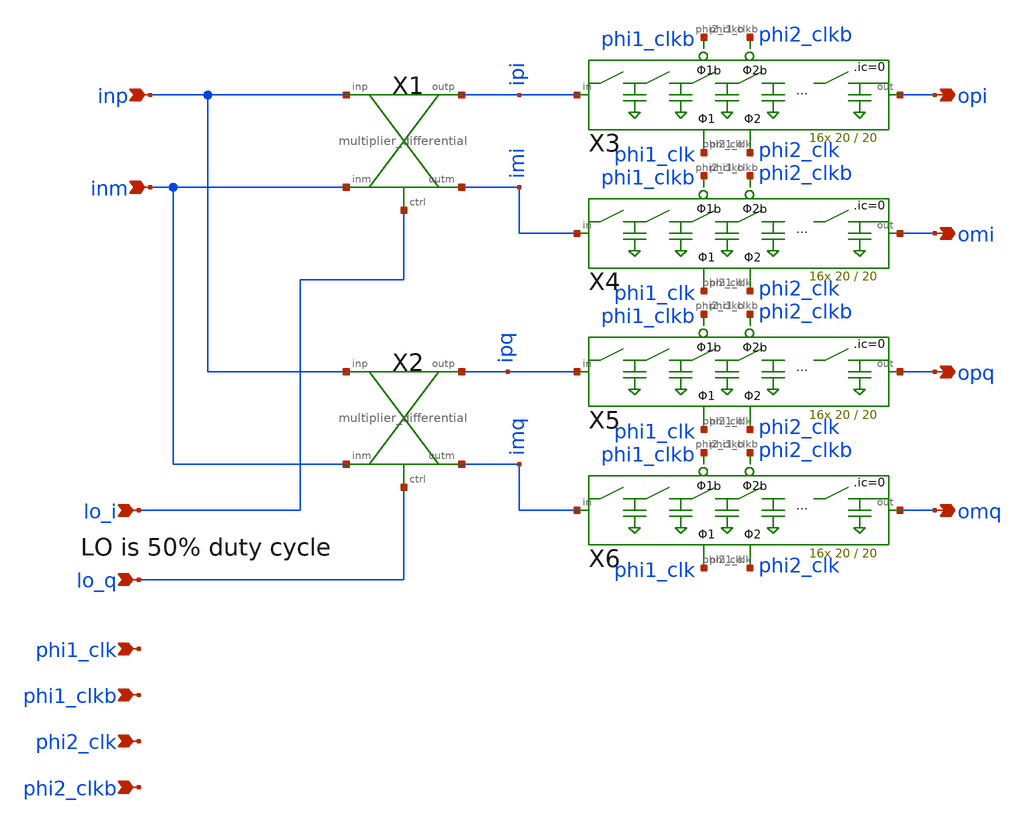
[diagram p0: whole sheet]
** sch_path: xschem/wavelet_channel/wavelet_iq.sch
**.subckt wavelet_iq inp inm phi1_clk phi2_clk lo_q lo_i opi omi opq omq phi1_clkb phi2_clkb
*.ipin inp
*.ipin inm
*.ipin phi1_clk
*.ipin phi2_clk
*.ipin lo_q
*.ipin lo_i
*.opin opi
*.opin omi
*.opin opq
*.opin omq
*.ipin phi1_clkb
*.ipin phi2_clkb
X1 inp ipi inm lo_i imi multiplier_differential
X2 inp ipq inm lo_q imq multiplier_differential
X3 ipi opi phi1_clk phi1_clkb phi2_clk phi2_clkb 16switchcaps_2phi W=20 L=20
X4 imi omi phi1_clk phi1_clkb phi2_clk phi2_clkb 16switchcaps_2phi W=20 L=20
X5 ipq opq phi1_clk phi1_clkb phi2_clk phi2_clkb 16switchcaps_2phi W=20 L=20
X6 imq omq phi1_clk phi1_clkb phi2_clk phi2_clkb 16switchcaps_2phi W=20 L=20
**.ends
.end
